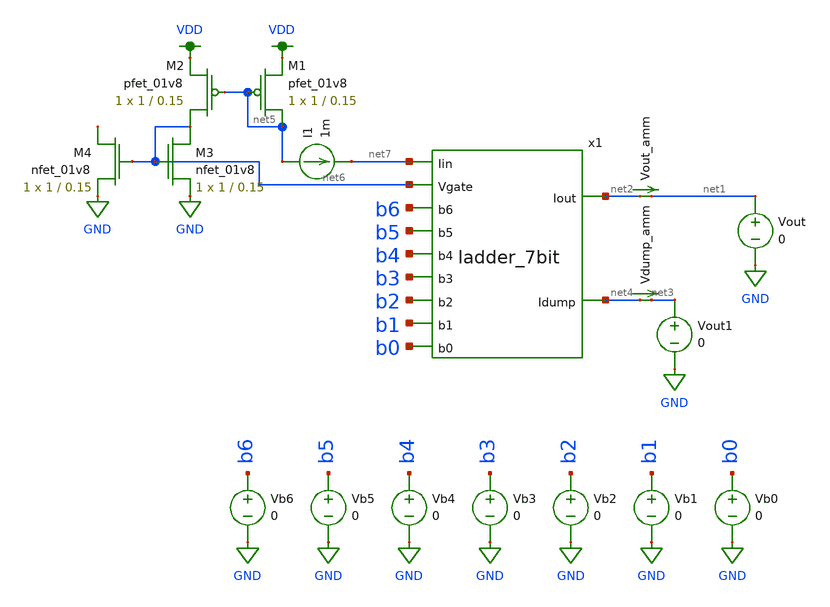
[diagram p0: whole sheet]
** sch_path: test_harness.sch
**.subckt test_harness
Vb0 b0 GND 0
Vb1 b1 GND 0
Vb2 b2 GND 0
Vb3 b3 GND 0
Vb4 b4 GND 0
Vb5 b5 GND 0
Vb6 b6 GND 0
Vout net1 GND 0
Vout1 net3 GND 0
Vout_amm net2 net1 0
.save i(vout_amm)
Vdump_amm net4 net3 0
.save i(vdump_amm)
I1 net5 net7 1m
XM1 net5 net5 VDD VDD sky130_fd_pr__pfet_01v8 L=0.15 W=1 nf=1 ad='int((nf+1)/2) * W/nf * 0.29' as='int((nf+2)/2) * W/nf * 0.29'
+ pd='2*int((nf+1)/2) * (W/nf + 0.29)' ps='2*int((nf+2)/2) * (W/nf + 0.29)' nrd='0.29 / W' nrs='0.29 / W'
+ sa=0 sb=0 sd=0 mult=1 m=1
XM2 net6 net5 VDD VDD sky130_fd_pr__pfet_01v8 L=0.15 W=1 nf=1 ad='int((nf+1)/2) * W/nf * 0.29' as='int((nf+2)/2) * W/nf * 0.29'
+ pd='2*int((nf+1)/2) * (W/nf + 0.29)' ps='2*int((nf+2)/2) * (W/nf + 0.29)' nrd='0.29 / W' nrs='0.29 / W'
+ sa=0 sb=0 sd=0 mult=1 m=1
XM3 net6 net6 GND GND sky130_fd_pr__nfet_01v8 L=0.15 W=1 nf=1 ad='int((nf+1)/2) * W/nf * 0.29' as='int((nf+2)/2) * W/nf * 0.29'
+ pd='2*int((nf+1)/2) * (W/nf + 0.29)' ps='2*int((nf+2)/2) * (W/nf + 0.29)' nrd='0.29 / W' nrs='0.29 / W'
+ sa=0 sb=0 sd=0 mult=1 m=1
XM4 net8 net6 GND GND sky130_fd_pr__nfet_01v8 L=0.15 W=1 nf=1 ad='int((nf+1)/2) * W/nf * 0.29' as='int((nf+2)/2) * W/nf * 0.29'
+ pd='2*int((nf+1)/2) * (W/nf + 0.29)' ps='2*int((nf+2)/2) * (W/nf + 0.29)' nrd='0.29 / W' nrs='0.29 / W'
+ sa=0 sb=0 sd=0 mult=1 m=1
x1 net6 net7 net4 net2 b5 b4 b1 b2 b3 b0 b6 ladder_7bit
**.ends
.GLOBAL GND
.GLOBAL VDD
.end
